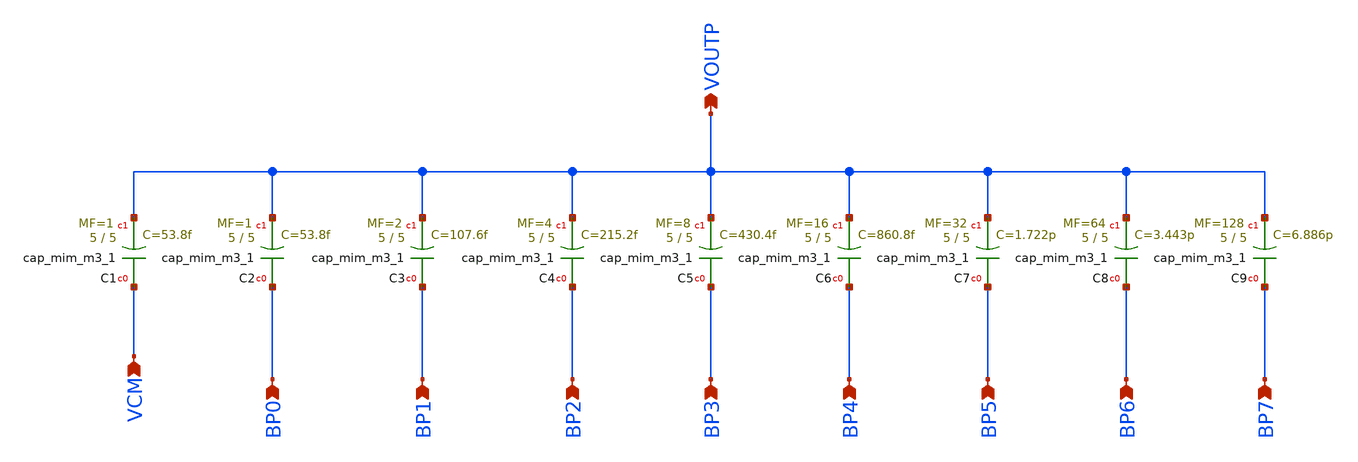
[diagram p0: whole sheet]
** sch_path: 02_sky130_pdk/soluzioni/lab_cdac/xschem/cdac.sch
**.subckt cdac VCM VOUTP BP0 BP1 BP2 BP3 BP4 BP5 BP6 BP7
*.ipin VCM
*.opin VOUTP
*.ipin BP0
*.ipin BP1
*.ipin BP2
*.ipin BP3
*.ipin BP4
*.ipin BP5
*.ipin BP6
*.ipin BP7
XC1 VCM VOUTP sky130_fd_pr__cap_mim_m3_1 W=5 L=5 MF=1 m=1
XC2 BP0 VOUTP sky130_fd_pr__cap_mim_m3_1 W=5 L=5 MF=1 m=1
XC3 BP1 VOUTP sky130_fd_pr__cap_mim_m3_1 W=5 L=5 MF=2 m=2
XC4 BP2 VOUTP sky130_fd_pr__cap_mim_m3_1 W=5 L=5 MF=4 m=4
XC5 BP3 VOUTP sky130_fd_pr__cap_mim_m3_1 W=5 L=5 MF=8 m=8
XC6 BP4 VOUTP sky130_fd_pr__cap_mim_m3_1 W=5 L=5 MF=16 m=16
XC7 BP5 VOUTP sky130_fd_pr__cap_mim_m3_1 W=5 L=5 MF=32 m=32
XC8 BP6 VOUTP sky130_fd_pr__cap_mim_m3_1 W=5 L=5 MF=64 m=64
XC9 BP7 VOUTP sky130_fd_pr__cap_mim_m3_1 W=5 L=5 MF=128 m=128
**.ends
.end
